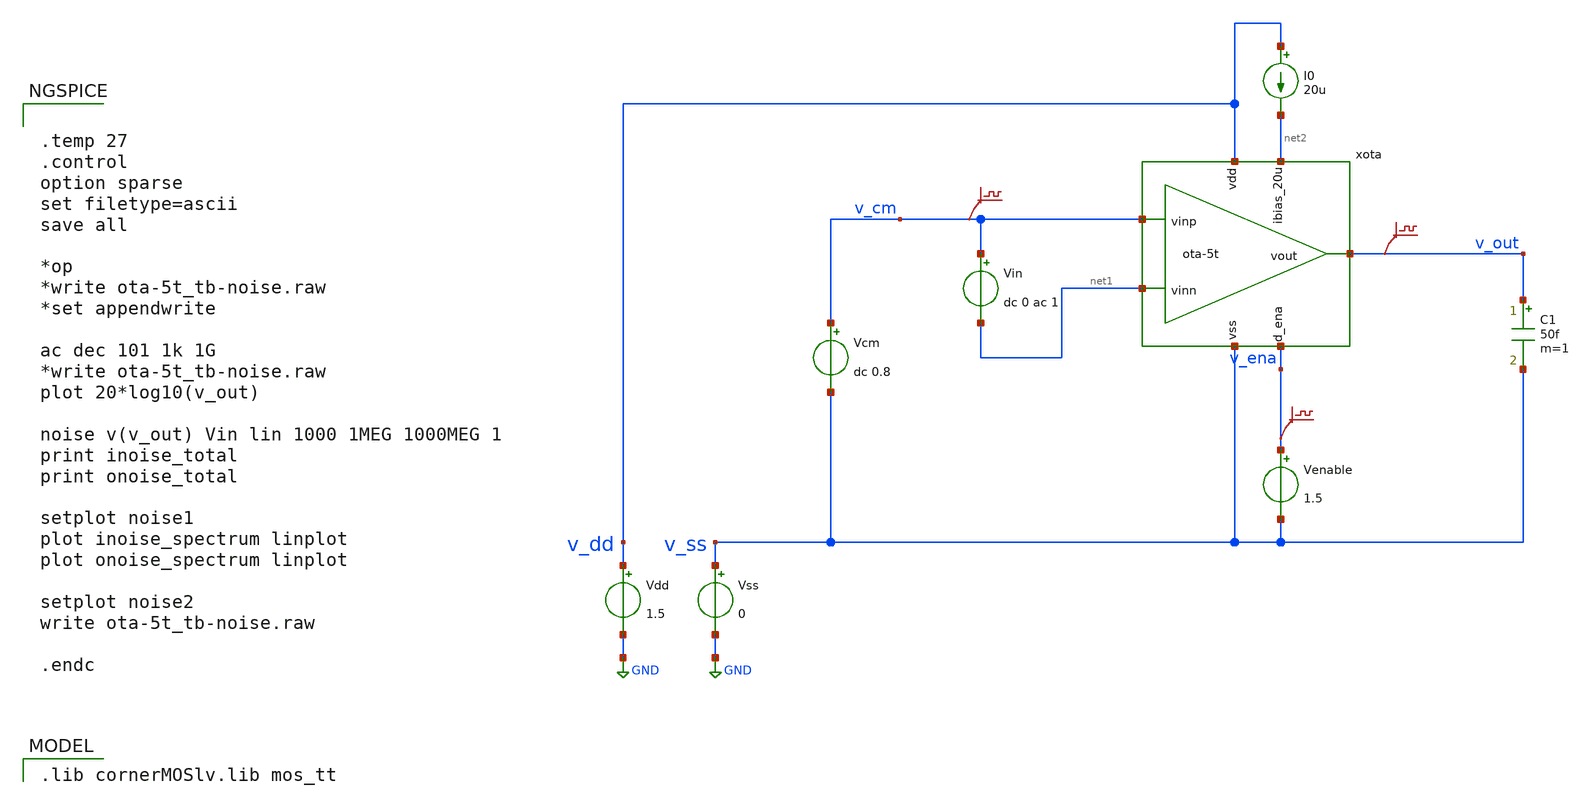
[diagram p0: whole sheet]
** sch_path: xschem/ota-5t_tb-noise.sch
* (c) 2024-2025 H. Pretl, Apache-2.0 license
**.subckt ota-5t_tb-noise
Vdd v_dd GND 1.5
xota v_dd v_out v_cm net1 net2 v_ena v_ss ota-5t
Vss v_ss GND 0
C1 v_out v_ss 50f m=1
Vcm v_cm v_ss dc 0.8
I0 v_dd net2 20u
Venable v_ena v_ss 1.5
.save v(v_cm)
.save v(v_out)
.save v(v_ena)
Vin v_cm net1 dc 0 ac 1
**** begin user architecture code
 .lib cornerMOSlv.lib mos_tt



.temp 27
.control
option sparse
set filetype=ascii
save all

*op
*write ota-5t_tb-noise.raw
*set appendwrite

ac dec 101 1k 1G
*write ota-5t_tb-noise.raw
plot 20*log10(v_out)

noise v(v_out) Vin lin 1000 1MEG 1000MEG 1
print inoise_total
print onoise_total

setplot noise1
plot inoise_spectrum linplot
plot onoise_spectrum linplot

setplot noise2
write ota-5t_tb-noise.raw

.endc


**** end user architecture code
**.ends
.GLOBAL GND
.end
